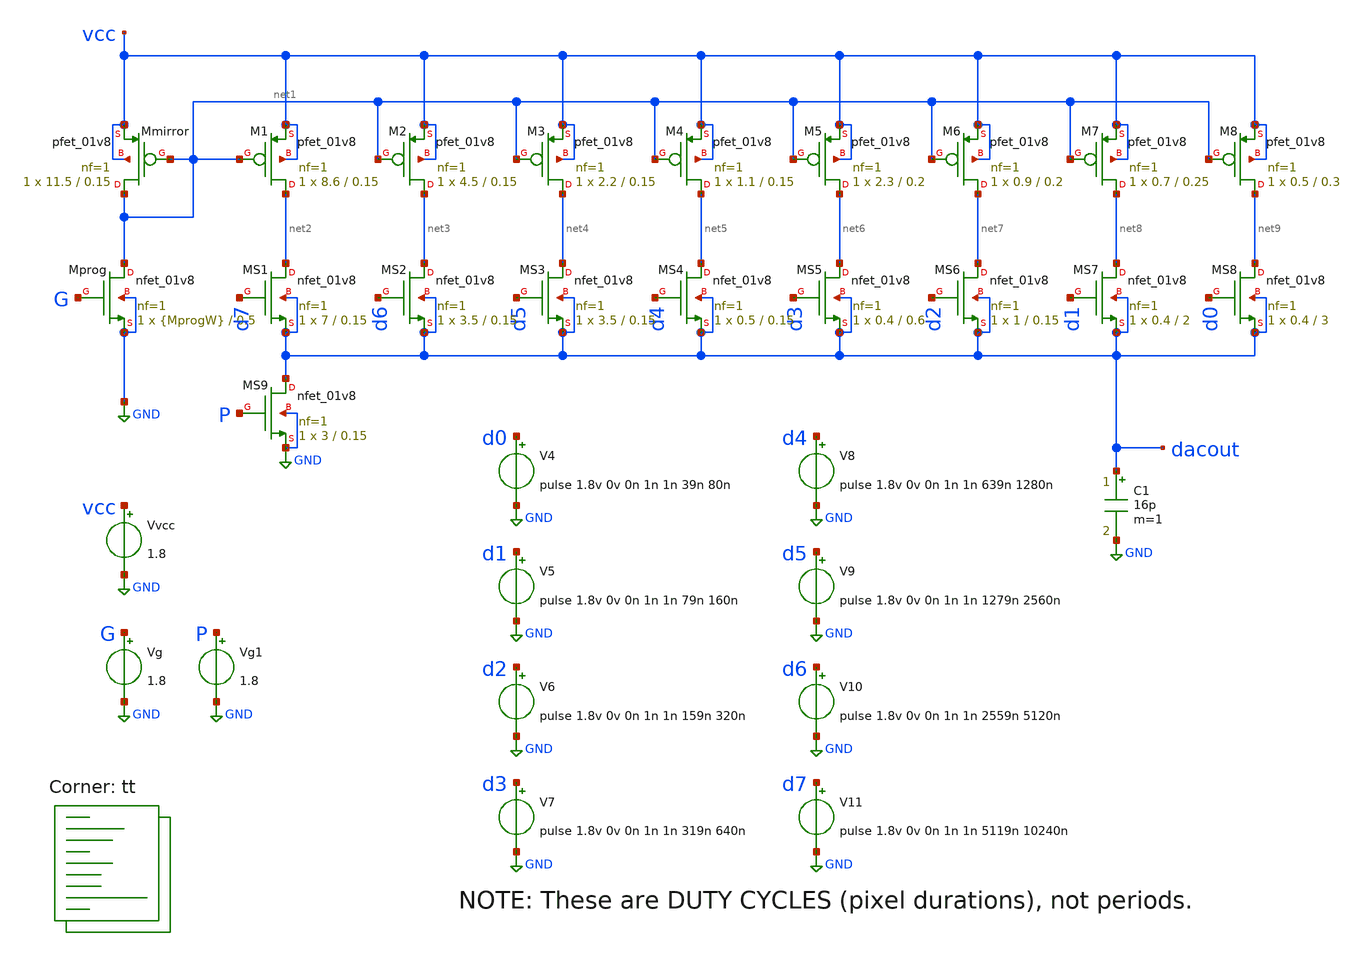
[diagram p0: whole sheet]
** sch_path: xschem/05b-moresweep.sch
**.subckt 05b-moresweep
Vvcc vcc GND 1.8
Vg G GND 1.8
XMprog net1 G GND GND sky130_fd_pr__nfet_01v8 L=0.5 W={MprogW} nf=1 ad='int((nf+1)/2) * W/nf * 0.29'
+ as='int((nf+2)/2) * W/nf * 0.29' pd='2*int((nf+1)/2) * (W/nf + 0.29)' ps='2*int((nf+2)/2) * (W/nf + 0.29)'
+ nrd='0.29 / W' nrs='0.29 / W' sa=0 sb=0 sd=0 mult=1 m=1
XMmirror net1 net1 vcc vcc sky130_fd_pr__pfet_01v8 L=0.15 W=11.5 nf=1 ad='int((nf+1)/2) * W/nf * 0.29'
+ as='int((nf+2)/2) * W/nf * 0.29' pd='2*int((nf+1)/2) * (W/nf + 0.29)' ps='2*int((nf+2)/2) * (W/nf + 0.29)'
+ nrd='0.29 / W' nrs='0.29 / W' sa=0 sb=0 sd=0 mult=1 m=1
XM1 net2 net1 vcc vcc sky130_fd_pr__pfet_01v8 L=0.15 W=8.6 nf=1 ad='int((nf+1)/2) * W/nf * 0.29' as='int((nf+2)/2) * W/nf * 0.29'
+ pd='2*int((nf+1)/2) * (W/nf + 0.29)' ps='2*int((nf+2)/2) * (W/nf + 0.29)' nrd='0.29 / W' nrs='0.29 / W'
+ sa=0 sb=0 sd=0 mult=1 m=1
XM2 net3 net1 vcc vcc sky130_fd_pr__pfet_01v8 L=0.15 W=4.5 nf=1 ad='int((nf+1)/2) * W/nf * 0.29' as='int((nf+2)/2) * W/nf * 0.29'
+ pd='2*int((nf+1)/2) * (W/nf + 0.29)' ps='2*int((nf+2)/2) * (W/nf + 0.29)' nrd='0.29 / W' nrs='0.29 / W'
+ sa=0 sb=0 sd=0 mult=1 m=1
XM3 net4 net1 vcc vcc sky130_fd_pr__pfet_01v8 L=0.15 W=2.2 nf=1 ad='int((nf+1)/2) * W/nf * 0.29' as='int((nf+2)/2) * W/nf * 0.29'
+ pd='2*int((nf+1)/2) * (W/nf + 0.29)' ps='2*int((nf+2)/2) * (W/nf + 0.29)' nrd='0.29 / W' nrs='0.29 / W'
+ sa=0 sb=0 sd=0 mult=1 m=1
XM4 net5 net1 vcc vcc sky130_fd_pr__pfet_01v8 L=0.15 W=1.1 nf=1 ad='int((nf+1)/2) * W/nf * 0.29' as='int((nf+2)/2) * W/nf * 0.29'
+ pd='2*int((nf+1)/2) * (W/nf + 0.29)' ps='2*int((nf+2)/2) * (W/nf + 0.29)' nrd='0.29 / W' nrs='0.29 / W'
+ sa=0 sb=0 sd=0 mult=1 m=1
XM5 net6 net1 vcc vcc sky130_fd_pr__pfet_01v8 L=0.2 W=2.3 nf=1 ad='int((nf+1)/2) * W/nf * 0.29' as='int((nf+2)/2) * W/nf * 0.29'
+ pd='2*int((nf+1)/2) * (W/nf + 0.29)' ps='2*int((nf+2)/2) * (W/nf + 0.29)' nrd='0.29 / W' nrs='0.29 / W'
+ sa=0 sb=0 sd=0 mult=1 m=1
XM6 net7 net1 vcc vcc sky130_fd_pr__pfet_01v8 L=0.2 W=0.9 nf=1 ad='int((nf+1)/2) * W/nf * 0.29' as='int((nf+2)/2) * W/nf * 0.29'
+ pd='2*int((nf+1)/2) * (W/nf + 0.29)' ps='2*int((nf+2)/2) * (W/nf + 0.29)' nrd='0.29 / W' nrs='0.29 / W'
+ sa=0 sb=0 sd=0 mult=1 m=1
XM7 net8 net1 vcc vcc sky130_fd_pr__pfet_01v8 L=0.25 W=0.7 nf=1 ad='int((nf+1)/2) * W/nf * 0.29' as='int((nf+2)/2) * W/nf * 0.29'
+ pd='2*int((nf+1)/2) * (W/nf + 0.29)' ps='2*int((nf+2)/2) * (W/nf + 0.29)' nrd='0.29 / W' nrs='0.29 / W'
+ sa=0 sb=0 sd=0 mult=1 m=1
XM8 net9 net1 vcc vcc sky130_fd_pr__pfet_01v8 L=0.3 W=0.5 nf=1 ad='int((nf+1)/2) * W/nf * 0.29' as='int((nf+2)/2) * W/nf * 0.29'
+ pd='2*int((nf+1)/2) * (W/nf + 0.29)' ps='2*int((nf+2)/2) * (W/nf + 0.29)' nrd='0.29 / W' nrs='0.29 / W'
+ sa=0 sb=0 sd=0 mult=1 m=1
XMS1 net2 d7 dacout dacout sky130_fd_pr__nfet_01v8 L=0.15 W=7 nf=1 ad='int((nf+1)/2) * W/nf * 0.29' as='int((nf+2)/2) * W/nf * 0.29'
+ pd='2*int((nf+1)/2) * (W/nf + 0.29)' ps='2*int((nf+2)/2) * (W/nf + 0.29)' nrd='0.29 / W' nrs='0.29 / W'
+ sa=0 sb=0 sd=0 mult=1 m=1
XMS2 net3 d6 dacout dacout sky130_fd_pr__nfet_01v8 L=0.15 W=3.5 nf=1 ad='int((nf+1)/2) * W/nf * 0.29'
+ as='int((nf+2)/2) * W/nf * 0.29' pd='2*int((nf+1)/2) * (W/nf + 0.29)' ps='2*int((nf+2)/2) * (W/nf + 0.29)'
+ nrd='0.29 / W' nrs='0.29 / W' sa=0 sb=0 sd=0 mult=1 m=1
XMS3 net4 d5 dacout dacout sky130_fd_pr__nfet_01v8 L=0.15 W=3.5 nf=1 ad='int((nf+1)/2) * W/nf * 0.29'
+ as='int((nf+2)/2) * W/nf * 0.29' pd='2*int((nf+1)/2) * (W/nf + 0.29)' ps='2*int((nf+2)/2) * (W/nf + 0.29)'
+ nrd='0.29 / W' nrs='0.29 / W' sa=0 sb=0 sd=0 mult=1 m=1
XMS4 net5 d4 dacout dacout sky130_fd_pr__nfet_01v8 L=0.15 W=0.5 nf=1 ad='int((nf+1)/2) * W/nf * 0.29'
+ as='int((nf+2)/2) * W/nf * 0.29' pd='2*int((nf+1)/2) * (W/nf + 0.29)' ps='2*int((nf+2)/2) * (W/nf + 0.29)'
+ nrd='0.29 / W' nrs='0.29 / W' sa=0 sb=0 sd=0 mult=1 m=1
XMS5 net6 d3 dacout dacout sky130_fd_pr__nfet_01v8 L=0.6 W=0.4 nf=1 ad='int((nf+1)/2) * W/nf * 0.29'
+ as='int((nf+2)/2) * W/nf * 0.29' pd='2*int((nf+1)/2) * (W/nf + 0.29)' ps='2*int((nf+2)/2) * (W/nf + 0.29)'
+ nrd='0.29 / W' nrs='0.29 / W' sa=0 sb=0 sd=0 mult=1 m=1
XMS6 net7 d2 dacout dacout sky130_fd_pr__nfet_01v8 L=0.15 W=1 nf=1 ad='int((nf+1)/2) * W/nf * 0.29' as='int((nf+2)/2) * W/nf * 0.29'
+ pd='2*int((nf+1)/2) * (W/nf + 0.29)' ps='2*int((nf+2)/2) * (W/nf + 0.29)' nrd='0.29 / W' nrs='0.29 / W'
+ sa=0 sb=0 sd=0 mult=1 m=1
XMS7 net8 d1 dacout dacout sky130_fd_pr__nfet_01v8 L=2 W=0.4 nf=1 ad='int((nf+1)/2) * W/nf * 0.29' as='int((nf+2)/2) * W/nf * 0.29'
+ pd='2*int((nf+1)/2) * (W/nf + 0.29)' ps='2*int((nf+2)/2) * (W/nf + 0.29)' nrd='0.29 / W' nrs='0.29 / W'
+ sa=0 sb=0 sd=0 mult=1 m=1
XMS8 net9 d0 dacout dacout sky130_fd_pr__nfet_01v8 L=3 W=0.4 nf=1 ad='int((nf+1)/2) * W/nf * 0.29' as='int((nf+2)/2) * W/nf * 0.29'
+ pd='2*int((nf+1)/2) * (W/nf + 0.29)' ps='2*int((nf+2)/2) * (W/nf + 0.29)' nrd='0.29 / W' nrs='0.29 / W'
+ sa=0 sb=0 sd=0 mult=1 m=1
V4 d0 GND pulse 1.8v 0v 0n 1n 1n 39n 80n
V5 d1 GND pulse 1.8v 0v 0n 1n 1n 79n 160n
V6 d2 GND pulse 1.8v 0v 0n 1n 1n 159n 320n
V7 d3 GND pulse 1.8v 0v 0n 1n 1n 319n 640n
V8 d4 GND pulse 1.8v 0v 0n 1n 1n 639n 1280n
V9 d5 GND pulse 1.8v 0v 0n 1n 1n 1279n 2560n
V10 d6 GND pulse 1.8v 0v 0n 1n 1n 2559n 5120n
V11 d7 GND pulse 1.8v 0v 0n 1n 1n 5119n 10240n
Vg1 P GND 1.8
XMS9 dacout P GND GND sky130_fd_pr__nfet_01v8 L=0.15 W=3 nf=1 ad='int((nf+1)/2) * W/nf * 0.29' as='int((nf+2)/2) * W/nf * 0.29'
+ pd='2*int((nf+1)/2) * (W/nf + 0.29)' ps='2*int((nf+2)/2) * (W/nf + 0.29)' nrd='0.29 / W' nrs='0.29 / W'
+ sa=0 sb=0 sd=0 mult=1 m=1
C1 dacout GND 16p m=1
**** begin user architecture code



.param MprogW=0.5
.options savecurrents
.control

*  set temp=90
  save all
  tran 1n 12.8u
  write 05.raw v(dacout)

  set appendwrite
  alterparam MprogW=0.55
  reset
  tran 1n 12.8u
  write 05.raw v(dacout)

  set appendwrite
  alterparam MprogW=0.6
  reset
  tran 1n 12.8u
  write 05.raw v(dacout)

  set appendwrite
  alterparam MprogW=0.65
  reset
  tran 1n 12.8u
  write 05.raw v(dacout)

  set appendwrite
  alterparam MprogW=0.7
  reset
  tran 1n 12.8u
  write 05.raw v(dacout)

  set appendwrite
  alterparam MprogW=0.75
  reset
  tran 1n 12.8u
  write 05.raw v(dacout)

  set appendwrite
  alterparam MprogW=0.8
  reset
  tran 1n 12.8u
  write 05.raw v(dacout)

  set appendwrite
  alterparam MprogW=0.85
  reset
  tran 1n 12.8u
  write 05.raw v(dacout)

  set appendwrite
  alterparam MprogW=0.9
  reset
  tran 1n 12.8u
  write 05.raw v(dacout)

  set appendwrite
  alterparam MprogW=0.95
  reset
  tran 1n 12.8u
  write 05.raw v(dacout)

  set appendwrite
  alterparam MprogW=1
  reset
  tran 1n 12.8u
  write 05.raw v(dacout)

  set appendwrite
  alterparam MprogW=1.05
  reset
  tran 1n 12.8u
  write 05.raw v(dacout)

  set appendwrite
  alterparam MprogW=1.1
  reset
  tran 1n 12.8u
  write 05.raw v(dacout)

  set appendwrite
  alterparam MprogW=1.15
  reset
  tran 1n 12.8u
  write 05.raw v(dacout)

  set appendwrite
  alterparam MprogW=1.2
  reset
  tran 1n 12.8u
  write 05.raw v(dacout)


.endc



.lib $::SKYWATER_MODELS/sky130.lib.spice tt
**** end user architecture code
**.ends
.GLOBAL GND
.end
